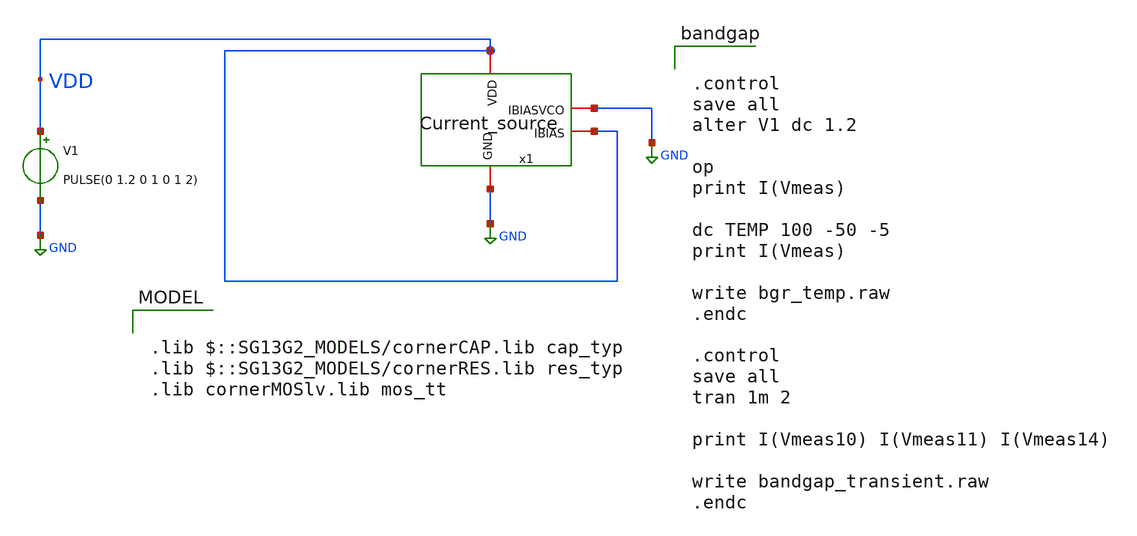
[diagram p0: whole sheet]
** sch_path: schematic/lc-vco/current_source/current_source_tb.sch
**.subckt current_source_tb
V1 VDD GND PULSE(0 1.2 0 1 0 1 2)
x1 GND VDD VDD GND Current_source
**** begin user architecture code

.lib $::SG13G2_MODELS/cornerCAP.lib cap_typ
.lib $::SG13G2_MODELS/cornerRES.lib res_typ
.lib cornerMOSlv.lib mos_tt



.control
save all
alter V1 dc 1.2

op
print I(Vmeas)

dc TEMP 100 -50 -5
print I(Vmeas)

write bgr_temp.raw
.endc

.control
save all
tran 1m 2

print I(Vmeas10) I(Vmeas11) I(Vmeas14)

write bandgap_transient.raw
.endc


**** end user architecture code
**.ends
.GLOBAL GND
.end
